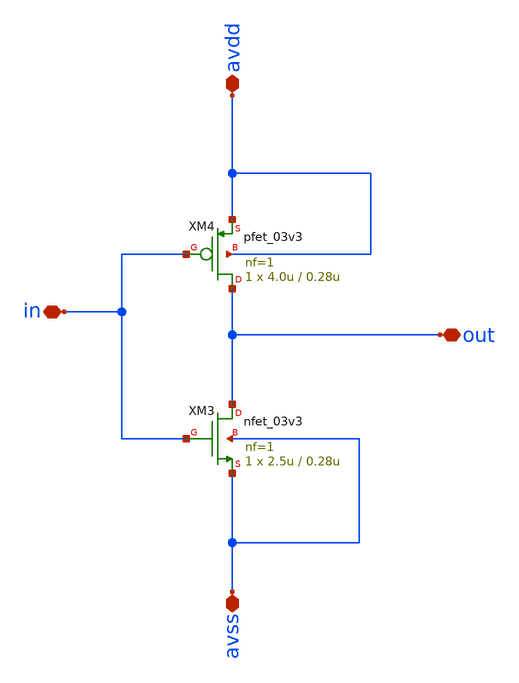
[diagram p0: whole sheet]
** sch_path: designs/libs/WK_Kadam/inv_test.sch
**.subckt inv_test avdd avss in out
*.iopin avdd
*.iopin avss
*.iopin in
*.iopin out
XM3 out in avss avss nfet_03v3 L=0.28u W=2.5u nf=1 ad='int((nf+1)/2) * W/nf * 0.18u' as='int((nf+2)/2) * W/nf * 0.18u'
+ pd='2*int((nf+1)/2) * (W/nf + 0.18u)' ps='2*int((nf+2)/2) * (W/nf + 0.18u)' nrd='0.18u / W' nrs='0.18u / W'
+ sa=0 sb=0 sd=0 m=1
XM4 out in avdd avdd pfet_03v3 L=0.28u W=4.0u nf=1 ad='int((nf+1)/2) * W/nf * 0.18u' as='int((nf+2)/2) * W/nf * 0.18u'
+ pd='2*int((nf+1)/2) * (W/nf + 0.18u)' ps='2*int((nf+2)/2) * (W/nf + 0.18u)' nrd='0.18u / W' nrs='0.18u / W'
+ sa=0 sb=0 sd=0 m=1
**.ends
.end
